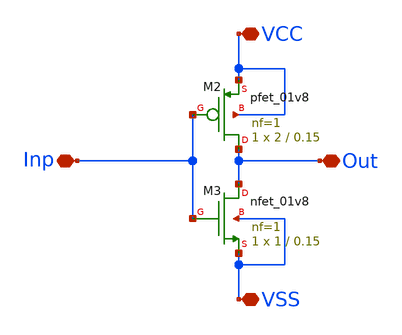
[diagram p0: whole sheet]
** sch_path: xschem/Inverter.sch
**.subckt Inverter Inp VSS Out VCC
*.iopin Inp
*.iopin VSS
*.iopin Out
*.iopin VCC
XM2 Out Inp VCC VCC sky130_fd_pr__pfet_01v8 L=0.15 W=2 nf=1 ad='int((1 + 1)/2) * 2 / 1 * 0.29' as='int((1 + 2)/2) * 2 / 1 * 0.29'
+ pd='2*int((1 + 1)/2) * (2 / 1 + 0.29)' ps='2*int((1 + 2)/2) * (2 / 1 + 0.29)' nrd='0.29 / 2 ' nrs='0.29 / 2 '
+ sa=0 sb=0 sd=0 mult=1 m=1
XM3 Out Inp VSS VSS sky130_fd_pr__nfet_01v8 L=0.15 W=1 nf=1 ad='int((1 + 1)/2) * 1 / 1 * 0.29' as='int((1 + 2)/2) * 1 / 1 * 0.29'
+ pd='2*int((1 + 1)/2) * (1 / 1 + 0.29)' ps='2*int((1 + 2)/2) * (1 / 1 + 0.29)' nrd='0.29 / 1 ' nrs='0.29 / 1 '
+ sa=0 sb=0 sd=0 mult=1 m=1
**.ends
.end
